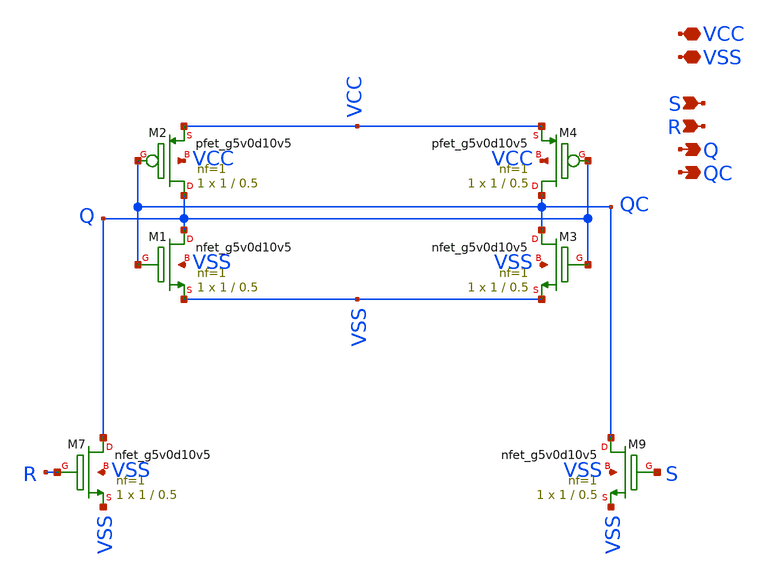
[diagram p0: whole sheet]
** sch_path: Comparator/schematic/miyahara/SR_latch.sch
**.subckt SR_latch VCC Q S R VSS QC
*.iopin VCC
*.opin Q
*.ipin S
*.ipin R
*.iopin VSS
*.opin QC
XM1 Q QC VSS VSS sky130_fd_pr__nfet_g5v0d10v5 L=0.5 W=1 nf=1 ad='int((nf+1)/2) * W/nf * 0.29' as='int((nf+2)/2) * W/nf * 0.29'
+ pd='2*int((nf+1)/2) * (W/nf + 0.29)' ps='2*int((nf+2)/2) * (W/nf + 0.29)' nrd='0.29 / W' nrs='0.29 / W'
+ sa=0 sb=0 sd=0 mult=1 m=1
XM2 Q QC VCC VCC sky130_fd_pr__pfet_g5v0d10v5 L=0.5 W=1 nf=1 ad='int((nf+1)/2) * W/nf * 0.29' as='int((nf+2)/2) * W/nf * 0.29'
+ pd='2*int((nf+1)/2) * (W/nf + 0.29)' ps='2*int((nf+2)/2) * (W/nf + 0.29)' nrd='0.29 / W' nrs='0.29 / W'
+ sa=0 sb=0 sd=0 mult=1 m=1
XM3 QC Q VSS VSS sky130_fd_pr__nfet_g5v0d10v5 L=0.5 W=1 nf=1 ad='int((nf+1)/2) * W/nf * 0.29' as='int((nf+2)/2) * W/nf * 0.29'
+ pd='2*int((nf+1)/2) * (W/nf + 0.29)' ps='2*int((nf+2)/2) * (W/nf + 0.29)' nrd='0.29 / W' nrs='0.29 / W'
+ sa=0 sb=0 sd=0 mult=1 m=1
XM4 QC Q VCC VCC sky130_fd_pr__pfet_g5v0d10v5 L=0.5 W=1 nf=1 ad='int((nf+1)/2) * W/nf * 0.29' as='int((nf+2)/2) * W/nf * 0.29'
+ pd='2*int((nf+1)/2) * (W/nf + 0.29)' ps='2*int((nf+2)/2) * (W/nf + 0.29)' nrd='0.29 / W' nrs='0.29 / W'
+ sa=0 sb=0 sd=0 mult=1 m=1
XM7 Q R VSS VSS sky130_fd_pr__nfet_g5v0d10v5 L=0.5 W=1 nf=1 ad='int((nf+1)/2) * W/nf * 0.29' as='int((nf+2)/2) * W/nf * 0.29'
+ pd='2*int((nf+1)/2) * (W/nf + 0.29)' ps='2*int((nf+2)/2) * (W/nf + 0.29)' nrd='0.29 / W' nrs='0.29 / W'
+ sa=0 sb=0 sd=0 mult=1 m=1
XM9 QC S VSS VSS sky130_fd_pr__nfet_g5v0d10v5 L=0.5 W=1 nf=1 ad='int((nf+1)/2) * W/nf * 0.29' as='int((nf+2)/2) * W/nf * 0.29'
+ pd='2*int((nf+1)/2) * (W/nf + 0.29)' ps='2*int((nf+2)/2) * (W/nf + 0.29)' nrd='0.29 / W' nrs='0.29 / W'
+ sa=0 sb=0 sd=0 mult=1 m=1
**.ends
.end
